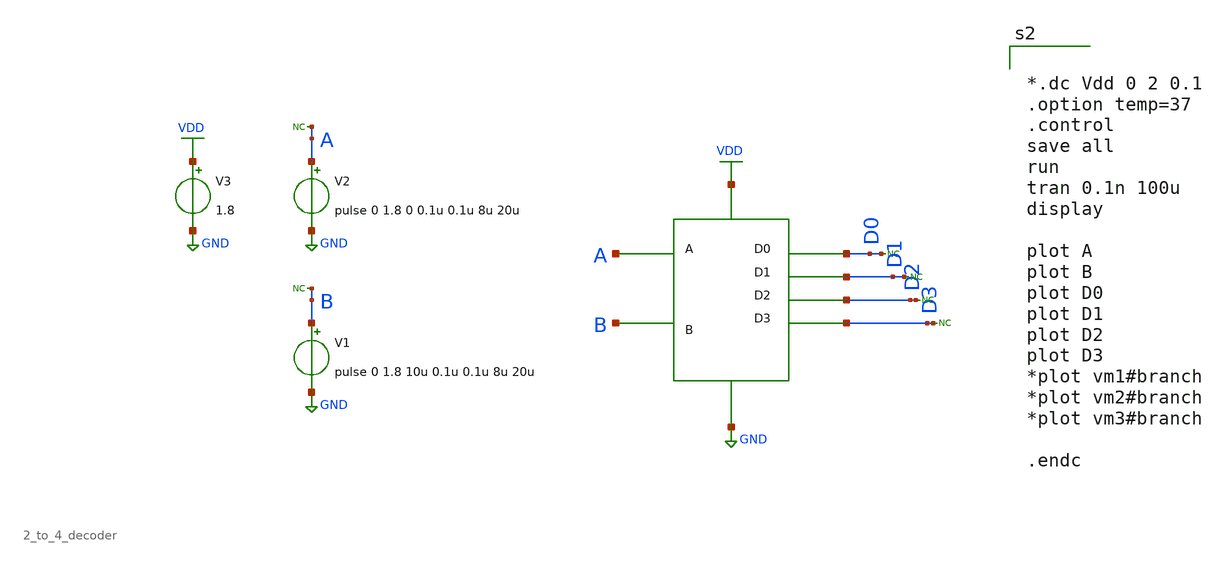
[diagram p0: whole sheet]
** sch_path: xschem/ip_block/logic_gate/tb_2_to_4_decoder.sch
**.subckt tb_2_to_4_decoder
V1 B GND pulse 0 1.8 10u 0.1u 0.1u 8u 20u
* noconn B
V2 A GND pulse 0 1.8 0 0.1u 0.1u 8u 20u
* noconn A
V3 VDD GND 1.8
X1 A GND VDD B D0 D1 D2 D3 2_to_4_decoder
* noconn D0
* noconn D1
* noconn D2
* noconn D3
**** begin user architecture code

** opencircuitdesign pdks install
.lib $::SKYWATER_MODELS/sky130.lib.spice tt




*.dc Vdd 0 2 0.1
.option temp=37
.control
save all
run
tran 0.1n 100u
display

plot A
plot B
plot D0
plot D1
plot D2
plot D3
*plot vm1#branch
*plot vm2#branch
*plot vm3#branch

.endc


**** end user architecture code
**.ends
.GLOBAL GND
.GLOBAL VDD
.end
